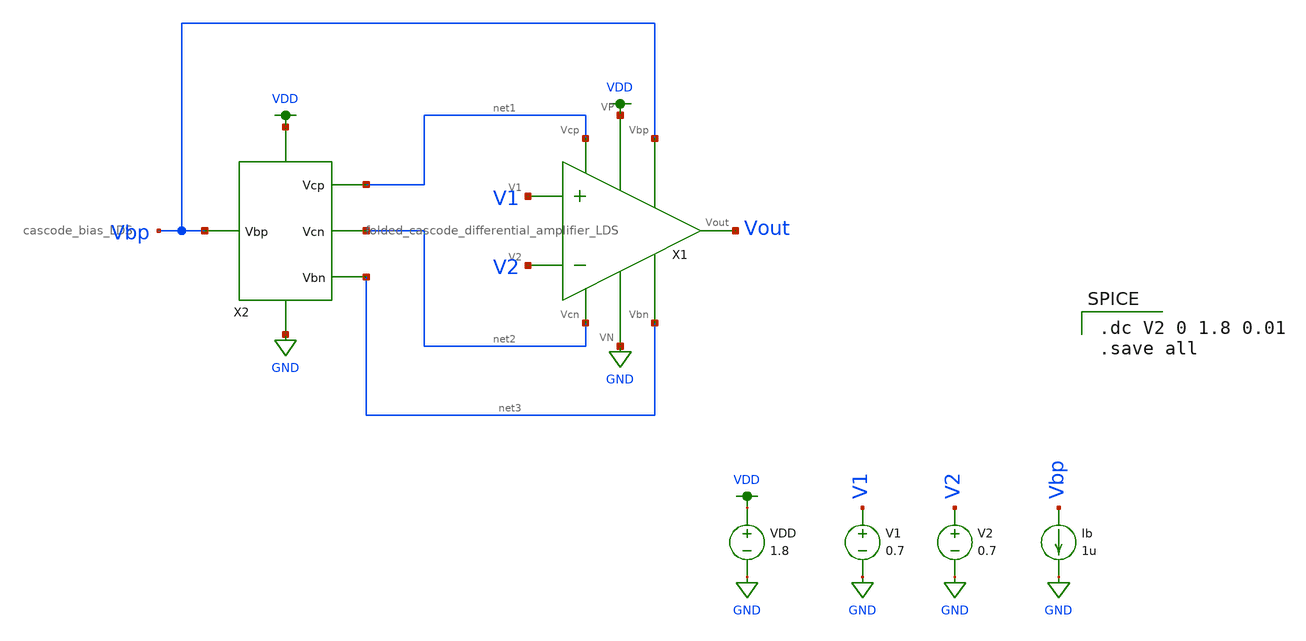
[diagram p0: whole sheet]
** sch_path: schematic/folded_cascode_simulation.sch
**.subckt folded_cascode_simulation
X1 VDD Vbp net1 Vout net3 net2 V1 V2 GND folded_cascode_differential_amplifier_LDS
X2 VDD net1 Vbp net2 net3 GND cascode_bias_LDS
VDD VDD GND 1.8
V1 V1 GND 0.7
V2 V2 GND 0.7
Ib Vbp GND 1u
**** begin user architecture code

.option wnflag=1
.lib ~/skywater/skywater-pdk/libraries/sky130_fd_pr_ngspice/latest/models/sky130.lib.spice tt


.dc V2 0 1.8 0.01
.save all

**** end user architecture code
**.ends

* expanding   symbol:
*+  /home/madvlsi/Documents/MADVLSI-MP3/schematic/folded_cascode_differential_amplifier_LDS.sym # of pins=9
** sym_path: schematic/folded_cascode_differential_amplifier_LDS.sym
** sch_path: schematic/folded_cascode_differential_amplifier_LDS.sch
.subckt folded_cascode_differential_amplifier_LDS VP Vbp Vcp Vout Vbn Vcn V1 V2 VN
*.ipin Vbn
*.ipin Vcn
*.ipin Vcp
*.ipin V2
*.ipin V1
*.ipin Vbp
*.iopin VP
*.iopin VN
*.opin Vout
XM5a net3 Vcn net6 GND sky130_fd_pr__nfet_01v8 L=0.5 W=6 nf=1 ad='int((nf+1)/2) * W/nf * 0.29' as='int((nf+2)/2) * W/nf * 0.29'
+ pd='2*int((nf+1)/2) * (W/nf + 0.29)' ps='2*int((nf+2)/2) * (W/nf + 0.29)' nrd='0.29 / W' nrs='0.29 / W'
+ sa=0 sb=0 sd=0 mult=1 m=1
XM1a net3 V1 net1 VDD sky130_fd_pr__pfet_01v8 L=0.5 W=3 nf=1 ad='int((nf+1)/2) * W/nf * 0.29' as='int((nf+2)/2) * W/nf * 0.29'
+ pd='2*int((nf+1)/2) * (W/nf + 0.29)' ps='2*int((nf+2)/2) * (W/nf + 0.29)' nrd='0.29 / W' nrs='0.29 / W'
+ sa=0 sb=0 sd=0 mult=1 m=1
XM2a net2 V2 net1 VDD sky130_fd_pr__pfet_01v8 L=0.5 W=3 nf=1 ad='int((nf+1)/2) * W/nf * 0.29' as='int((nf+2)/2) * W/nf * 0.29'
+ pd='2*int((nf+1)/2) * (W/nf + 0.29)' ps='2*int((nf+2)/2) * (W/nf + 0.29)' nrd='0.29 / W' nrs='0.29 / W'
+ sa=0 sb=0 sd=0 mult=1 m=1
XM2b net1 V2 net2 VDD sky130_fd_pr__pfet_01v8 L=0.5 W=3 nf=1 ad='int((nf+1)/2) * W/nf * 0.29' as='int((nf+2)/2) * W/nf * 0.29'
+ pd='2*int((nf+1)/2) * (W/nf + 0.29)' ps='2*int((nf+2)/2) * (W/nf + 0.29)' nrd='0.29 / W' nrs='0.29 / W'
+ sa=0 sb=0 sd=0 mult=1 m=1
XM1b net1 V1 net3 VDD sky130_fd_pr__pfet_01v8 L=0.5 W=3 nf=1 ad='int((nf+1)/2) * W/nf * 0.29' as='int((nf+2)/2) * W/nf * 0.29'
+ pd='2*int((nf+1)/2) * (W/nf + 0.29)' ps='2*int((nf+2)/2) * (W/nf + 0.29)' nrd='0.29 / W' nrs='0.29 / W'
+ sa=0 sb=0 sd=0 mult=1 m=1
XM1c net3 V1 net1 VDD sky130_fd_pr__pfet_01v8 L=0.5 W=3 nf=1 ad='int((nf+1)/2) * W/nf * 0.29' as='int((nf+2)/2) * W/nf * 0.29'
+ pd='2*int((nf+1)/2) * (W/nf + 0.29)' ps='2*int((nf+2)/2) * (W/nf + 0.29)' nrd='0.29 / W' nrs='0.29 / W'
+ sa=0 sb=0 sd=0 mult=1 m=1
XM2c net2 V2 net1 VDD sky130_fd_pr__pfet_01v8 L=0.5 W=3 nf=1 ad='int((nf+1)/2) * W/nf * 0.29' as='int((nf+2)/2) * W/nf * 0.29'
+ pd='2*int((nf+1)/2) * (W/nf + 0.29)' ps='2*int((nf+2)/2) * (W/nf + 0.29)' nrd='0.29 / W' nrs='0.29 / W'
+ sa=0 sb=0 sd=0 mult=1 m=1
XM2d net1 V2 net2 VDD sky130_fd_pr__pfet_01v8 L=0.5 W=3 nf=1 ad='int((nf+1)/2) * W/nf * 0.29' as='int((nf+2)/2) * W/nf * 0.29'
+ pd='2*int((nf+1)/2) * (W/nf + 0.29)' ps='2*int((nf+2)/2) * (W/nf + 0.29)' nrd='0.29 / W' nrs='0.29 / W'
+ sa=0 sb=0 sd=0 mult=1 m=1
XM1d net1 V1 net3 VDD sky130_fd_pr__pfet_01v8 L=0.5 W=3 nf=1 ad='int((nf+1)/2) * W/nf * 0.29' as='int((nf+2)/2) * W/nf * 0.29'
+ pd='2*int((nf+1)/2) * (W/nf + 0.29)' ps='2*int((nf+2)/2) * (W/nf + 0.29)' nrd='0.29 / W' nrs='0.29 / W'
+ sa=0 sb=0 sd=0 mult=1 m=1
XM11a VP Vbp net1 VDD sky130_fd_pr__pfet_01v8 L=0.5 W=1.5 nf=1 ad='int((nf+1)/2) * W/nf * 0.29' as='int((nf+2)/2) * W/nf * 0.29'
+ pd='2*int((nf+1)/2) * (W/nf + 0.29)' ps='2*int((nf+2)/2) * (W/nf + 0.29)' nrd='0.29 / W' nrs='0.29 / W'
+ sa=0 sb=0 sd=0 mult=1 m=1
XM11b net1 Vbp VP VDD sky130_fd_pr__pfet_01v8 L=0.5 W=1.5 nf=1 ad='int((nf+1)/2) * W/nf * 0.29' as='int((nf+2)/2) * W/nf * 0.29'
+ pd='2*int((nf+1)/2) * (W/nf + 0.29)' ps='2*int((nf+2)/2) * (W/nf + 0.29)' nrd='0.29 / W' nrs='0.29 / W'
+ sa=0 sb=0 sd=0 mult=1 m=1
XM11c VP Vbp net1 VDD sky130_fd_pr__pfet_01v8 L=0.5 W=1.5 nf=1 ad='int((nf+1)/2) * W/nf * 0.29' as='int((nf+2)/2) * W/nf * 0.29'
+ pd='2*int((nf+1)/2) * (W/nf + 0.29)' ps='2*int((nf+2)/2) * (W/nf + 0.29)' nrd='0.29 / W' nrs='0.29 / W'
+ sa=0 sb=0 sd=0 mult=1 m=1
XM11d net1 Vbp VP VDD sky130_fd_pr__pfet_01v8 L=0.5 W=1.5 nf=1 ad='int((nf+1)/2) * W/nf * 0.29' as='int((nf+2)/2) * W/nf * 0.29'
+ pd='2*int((nf+1)/2) * (W/nf + 0.29)' ps='2*int((nf+2)/2) * (W/nf + 0.29)' nrd='0.29 / W' nrs='0.29 / W'
+ sa=0 sb=0 sd=0 mult=1 m=1
XM11e VP Vbp net1 VDD sky130_fd_pr__pfet_01v8 L=0.5 W=1.5 nf=1 ad='int((nf+1)/2) * W/nf * 0.29' as='int((nf+2)/2) * W/nf * 0.29'
+ pd='2*int((nf+1)/2) * (W/nf + 0.29)' ps='2*int((nf+2)/2) * (W/nf + 0.29)' nrd='0.29 / W' nrs='0.29 / W'
+ sa=0 sb=0 sd=0 mult=1 m=1
XM11f net1 Vbp VP VDD sky130_fd_pr__pfet_01v8 L=0.5 W=1.5 nf=1 ad='int((nf+1)/2) * W/nf * 0.29' as='int((nf+2)/2) * W/nf * 0.29'
+ pd='2*int((nf+1)/2) * (W/nf + 0.29)' ps='2*int((nf+2)/2) * (W/nf + 0.29)' nrd='0.29 / W' nrs='0.29 / W'
+ sa=0 sb=0 sd=0 mult=1 m=1
XM11g VP Vbp net1 VDD sky130_fd_pr__pfet_01v8 L=0.5 W=1.5 nf=1 ad='int((nf+1)/2) * W/nf * 0.29' as='int((nf+2)/2) * W/nf * 0.29'
+ pd='2*int((nf+1)/2) * (W/nf + 0.29)' ps='2*int((nf+2)/2) * (W/nf + 0.29)' nrd='0.29 / W' nrs='0.29 / W'
+ sa=0 sb=0 sd=0 mult=1 m=1
XM11h net1 Vbp VP VDD sky130_fd_pr__pfet_01v8 L=0.5 W=1.5 nf=1 ad='int((nf+1)/2) * W/nf * 0.29' as='int((nf+2)/2) * W/nf * 0.29'
+ pd='2*int((nf+1)/2) * (W/nf + 0.29)' ps='2*int((nf+2)/2) * (W/nf + 0.29)' nrd='0.29 / W' nrs='0.29 / W'
+ sa=0 sb=0 sd=0 mult=1 m=1
XM3a VN Vbn net3 GND sky130_fd_pr__nfet_01v8 L=0.5 W=6 nf=1 ad='int((nf+1)/2) * W/nf * 0.29' as='int((nf+2)/2) * W/nf * 0.29'
+ pd='2*int((nf+1)/2) * (W/nf + 0.29)' ps='2*int((nf+2)/2) * (W/nf + 0.29)' nrd='0.29 / W' nrs='0.29 / W'
+ sa=0 sb=0 sd=0 mult=1 m=1
XM4a net2 Vbn VN GND sky130_fd_pr__nfet_01v8 L=0.5 W=6 nf=1 ad='int((nf+1)/2) * W/nf * 0.29' as='int((nf+2)/2) * W/nf * 0.29'
+ pd='2*int((nf+1)/2) * (W/nf + 0.29)' ps='2*int((nf+2)/2) * (W/nf + 0.29)' nrd='0.29 / W' nrs='0.29 / W'
+ sa=0 sb=0 sd=0 mult=1 m=1
XM6a Vout Vcn net2 GND sky130_fd_pr__nfet_01v8 L=0.5 W=6 nf=1 ad='int((nf+1)/2) * W/nf * 0.29' as='int((nf+2)/2) * W/nf * 0.29'
+ pd='2*int((nf+1)/2) * (W/nf + 0.29)' ps='2*int((nf+2)/2) * (W/nf + 0.29)' nrd='0.29 / W' nrs='0.29 / W'
+ sa=0 sb=0 sd=0 mult=1 m=1
XM6b net2 Vcn Vout GND sky130_fd_pr__nfet_01v8 L=0.5 W=6 nf=1 ad='int((nf+1)/2) * W/nf * 0.29' as='int((nf+2)/2) * W/nf * 0.29'
+ pd='2*int((nf+1)/2) * (W/nf + 0.29)' ps='2*int((nf+2)/2) * (W/nf + 0.29)' nrd='0.29 / W' nrs='0.29 / W'
+ sa=0 sb=0 sd=0 mult=1 m=1
XM4b VN Vbn net2 GND sky130_fd_pr__nfet_01v8 L=0.5 W=6 nf=1 ad='int((nf+1)/2) * W/nf * 0.29' as='int((nf+2)/2) * W/nf * 0.29'
+ pd='2*int((nf+1)/2) * (W/nf + 0.29)' ps='2*int((nf+2)/2) * (W/nf + 0.29)' nrd='0.29 / W' nrs='0.29 / W'
+ sa=0 sb=0 sd=0 mult=1 m=1
XM3b net3 Vbn VN GND sky130_fd_pr__nfet_01v8 L=0.5 W=6 nf=1 ad='int((nf+1)/2) * W/nf * 0.29' as='int((nf+2)/2) * W/nf * 0.29'
+ pd='2*int((nf+1)/2) * (W/nf + 0.29)' ps='2*int((nf+2)/2) * (W/nf + 0.29)' nrd='0.29 / W' nrs='0.29 / W'
+ sa=0 sb=0 sd=0 mult=1 m=1
XM5b net6 Vcn net3 GND sky130_fd_pr__nfet_01v8 L=0.5 W=6 nf=1 ad='int((nf+1)/2) * W/nf * 0.29' as='int((nf+2)/2) * W/nf * 0.29'
+ pd='2*int((nf+1)/2) * (W/nf + 0.29)' ps='2*int((nf+2)/2) * (W/nf + 0.29)' nrd='0.29 / W' nrs='0.29 / W'
+ sa=0 sb=0 sd=0 mult=1 m=1
XM10a Vout Vcp net4 VDD sky130_fd_pr__pfet_01v8 L=0.5 W=6 nf=1 ad='int((nf+1)/2) * W/nf * 0.29' as='int((nf+2)/2) * W/nf * 0.29'
+ pd='2*int((nf+1)/2) * (W/nf + 0.29)' ps='2*int((nf+2)/2) * (W/nf + 0.29)' nrd='0.29 / W' nrs='0.29 / W'
+ sa=0 sb=0 sd=0 mult=1 m=1
XM8a net4 net6 VP VDD sky130_fd_pr__pfet_01v8 L=0.5 W=6 nf=1 ad='int((nf+1)/2) * W/nf * 0.29' as='int((nf+2)/2) * W/nf * 0.29'
+ pd='2*int((nf+1)/2) * (W/nf + 0.29)' ps='2*int((nf+2)/2) * (W/nf + 0.29)' nrd='0.29 / W' nrs='0.29 / W'
+ sa=0 sb=0 sd=0 mult=1 m=1
XM7a VP net6 net5 VDD sky130_fd_pr__pfet_01v8 L=0.5 W=6 nf=1 ad='int((nf+1)/2) * W/nf * 0.29' as='int((nf+2)/2) * W/nf * 0.29'
+ pd='2*int((nf+1)/2) * (W/nf + 0.29)' ps='2*int((nf+2)/2) * (W/nf + 0.29)' nrd='0.29 / W' nrs='0.29 / W'
+ sa=0 sb=0 sd=0 mult=1 m=1
XM9a net5 Vcp net6 VDD sky130_fd_pr__pfet_01v8 L=0.5 W=6 nf=1 ad='int((nf+1)/2) * W/nf * 0.29' as='int((nf+2)/2) * W/nf * 0.29'
+ pd='2*int((nf+1)/2) * (W/nf + 0.29)' ps='2*int((nf+2)/2) * (W/nf + 0.29)' nrd='0.29 / W' nrs='0.29 / W'
+ sa=0 sb=0 sd=0 mult=1 m=1
XM9b net6 Vcp net5 VDD sky130_fd_pr__pfet_01v8 L=0.5 W=6 nf=1 ad='int((nf+1)/2) * W/nf * 0.29' as='int((nf+2)/2) * W/nf * 0.29'
+ pd='2*int((nf+1)/2) * (W/nf + 0.29)' ps='2*int((nf+2)/2) * (W/nf + 0.29)' nrd='0.29 / W' nrs='0.29 / W'
+ sa=0 sb=0 sd=0 mult=1 m=1
XM7b net5 net6 VP VDD sky130_fd_pr__pfet_01v8 L=0.5 W=6 nf=1 ad='int((nf+1)/2) * W/nf * 0.29' as='int((nf+2)/2) * W/nf * 0.29'
+ pd='2*int((nf+1)/2) * (W/nf + 0.29)' ps='2*int((nf+2)/2) * (W/nf + 0.29)' nrd='0.29 / W' nrs='0.29 / W'
+ sa=0 sb=0 sd=0 mult=1 m=1
XM8b VP net6 net4 VDD sky130_fd_pr__pfet_01v8 L=0.5 W=6 nf=1 ad='int((nf+1)/2) * W/nf * 0.29' as='int((nf+2)/2) * W/nf * 0.29'
+ pd='2*int((nf+1)/2) * (W/nf + 0.29)' ps='2*int((nf+2)/2) * (W/nf + 0.29)' nrd='0.29 / W' nrs='0.29 / W'
+ sa=0 sb=0 sd=0 mult=1 m=1
XM10b net4 Vcp Vout VDD sky130_fd_pr__pfet_01v8 L=0.5 W=6 nf=1 ad='int((nf+1)/2) * W/nf * 0.29' as='int((nf+2)/2) * W/nf * 0.29'
+ pd='2*int((nf+1)/2) * (W/nf + 0.29)' ps='2*int((nf+2)/2) * (W/nf + 0.29)' nrd='0.29 / W' nrs='0.29 / W'
+ sa=0 sb=0 sd=0 mult=1 m=1
XM15 net3 VP VP VDD sky130_fd_pr__pfet_01v8 L=0.5 W=3 nf=1 ad='int((nf+1)/2) * W/nf * 0.29' as='int((nf+2)/2) * W/nf * 0.29'
+ pd='2*int((nf+1)/2) * (W/nf + 0.29)' ps='2*int((nf+2)/2) * (W/nf + 0.29)' nrd='0.29 / W' nrs='0.29 / W'
+ sa=0 sb=0 sd=0 mult=1 m=1
XM14 VP VP net3 VDD sky130_fd_pr__pfet_01v8 L=0.5 W=3 nf=1 ad='int((nf+1)/2) * W/nf * 0.29' as='int((nf+2)/2) * W/nf * 0.29'
+ pd='2*int((nf+1)/2) * (W/nf + 0.29)' ps='2*int((nf+2)/2) * (W/nf + 0.29)' nrd='0.29 / W' nrs='0.29 / W'
+ sa=0 sb=0 sd=0 mult=1 m=1
XM13 VP VP VP VDD sky130_fd_pr__pfet_01v8 L=0.5 W=1.5 nf=1 ad='int((nf+1)/2) * W/nf * 0.29' as='int((nf+2)/2) * W/nf * 0.29'
+ pd='2*int((nf+1)/2) * (W/nf + 0.29)' ps='2*int((nf+2)/2) * (W/nf + 0.29)' nrd='0.29 / W' nrs='0.29 / W'
+ sa=0 sb=0 sd=0 mult=1 m=1
XM12 VP VP VP VDD sky130_fd_pr__pfet_01v8 L=0.5 W=1.5 nf=1 ad='int((nf+1)/2) * W/nf * 0.29' as='int((nf+2)/2) * W/nf * 0.29'
+ pd='2*int((nf+1)/2) * (W/nf + 0.29)' ps='2*int((nf+2)/2) * (W/nf + 0.29)' nrd='0.29 / W' nrs='0.29 / W'
+ sa=0 sb=0 sd=0 mult=1 m=1
XM16 VP VP Vout VDD sky130_fd_pr__pfet_01v8 L=0.5 W=6 nf=1 ad='int((nf+1)/2) * W/nf * 0.29' as='int((nf+2)/2) * W/nf * 0.29'
+ pd='2*int((nf+1)/2) * (W/nf + 0.29)' ps='2*int((nf+2)/2) * (W/nf + 0.29)' nrd='0.29 / W' nrs='0.29 / W'
+ sa=0 sb=0 sd=0 mult=1 m=1
XM17 Vout VP VP VDD sky130_fd_pr__pfet_01v8 L=0.5 W=6 nf=1 ad='int((nf+1)/2) * W/nf * 0.29' as='int((nf+2)/2) * W/nf * 0.29'
+ pd='2*int((nf+1)/2) * (W/nf + 0.29)' ps='2*int((nf+2)/2) * (W/nf + 0.29)' nrd='0.29 / W' nrs='0.29 / W'
+ sa=0 sb=0 sd=0 mult=1 m=1
XM19 VN VN net6 GND sky130_fd_pr__nfet_01v8 L=0.5 W=6 nf=1 ad='int((nf+1)/2) * W/nf * 0.29' as='int((nf+2)/2) * W/nf * 0.29'
+ pd='2*int((nf+1)/2) * (W/nf + 0.29)' ps='2*int((nf+2)/2) * (W/nf + 0.29)' nrd='0.29 / W' nrs='0.29 / W'
+ sa=0 sb=0 sd=0 mult=1 m=1
XM18 net6 VN VN GND sky130_fd_pr__nfet_01v8 L=0.5 W=6 nf=1 ad='int((nf+1)/2) * W/nf * 0.29' as='int((nf+2)/2) * W/nf * 0.29'
+ pd='2*int((nf+1)/2) * (W/nf + 0.29)' ps='2*int((nf+2)/2) * (W/nf + 0.29)' nrd='0.29 / W' nrs='0.29 / W'
+ sa=0 sb=0 sd=0 mult=1 m=1
.ends


* expanding   symbol:  /home/madvlsi/Documents/MADVLSI-MP3/schematic/cascode_bias_LDS.sym # of
*+ pins=6
** sym_path: schematic/cascode_bias_LDS.sym
** sch_path: schematic/cascode_bias_LDS.sch
.subckt cascode_bias_LDS VP Vcp Vbp Vcn Vbn VN
*.iopin VP
*.iopin VN
*.opin Vcp
*.opin Vbn
*.opin Vcn
*.iopin Vbp
XM1a VP Vbp Vbp VDD sky130_fd_pr__pfet_01v8 L=0.5 W=6 nf=1 ad='int((nf+1)/2) * W/nf * 0.29' as='int((nf+2)/2) * W/nf * 0.29'
+ pd='2*int((nf+1)/2) * (W/nf + 0.29)' ps='2*int((nf+2)/2) * (W/nf + 0.29)' nrd='0.29 / W' nrs='0.29 / W'
+ sa=0 sb=0 sd=0 mult=1 m=1
XM2a Vbn Vbp VP VDD sky130_fd_pr__pfet_01v8 L=0.5 W=6 nf=1 ad='int((nf+1)/2) * W/nf * 0.29' as='int((nf+2)/2) * W/nf * 0.29'
+ pd='2*int((nf+1)/2) * (W/nf + 0.29)' ps='2*int((nf+2)/2) * (W/nf + 0.29)' nrd='0.29 / W' nrs='0.29 / W'
+ sa=0 sb=0 sd=0 mult=1 m=1
XM3a VP Vbp Vcn VDD sky130_fd_pr__pfet_01v8 L=0.5 W=6 nf=1 ad='int((nf+1)/2) * W/nf * 0.29' as='int((nf+2)/2) * W/nf * 0.29'
+ pd='2*int((nf+1)/2) * (W/nf + 0.29)' ps='2*int((nf+2)/2) * (W/nf + 0.29)' nrd='0.29 / W' nrs='0.29 / W'
+ sa=0 sb=0 sd=0 mult=1 m=1
XM4a net1 Vbp VP VDD sky130_fd_pr__pfet_01v8 L=0.5 W=6 nf=1 ad='int((nf+1)/2) * W/nf * 0.29' as='int((nf+2)/2) * W/nf * 0.29'
+ pd='2*int((nf+1)/2) * (W/nf + 0.29)' ps='2*int((nf+2)/2) * (W/nf + 0.29)' nrd='0.29 / W' nrs='0.29 / W'
+ sa=0 sb=0 sd=0 mult=1 m=1
XM4b VP Vbp net1 VDD sky130_fd_pr__pfet_01v8 L=0.5 W=6 nf=1 ad='int((nf+1)/2) * W/nf * 0.29' as='int((nf+2)/2) * W/nf * 0.29'
+ pd='2*int((nf+1)/2) * (W/nf + 0.29)' ps='2*int((nf+2)/2) * (W/nf + 0.29)' nrd='0.29 / W' nrs='0.29 / W'
+ sa=0 sb=0 sd=0 mult=1 m=1
XM3b Vcn Vbp VP VDD sky130_fd_pr__pfet_01v8 L=0.5 W=6 nf=1 ad='int((nf+1)/2) * W/nf * 0.29' as='int((nf+2)/2) * W/nf * 0.29'
+ pd='2*int((nf+1)/2) * (W/nf + 0.29)' ps='2*int((nf+2)/2) * (W/nf + 0.29)' nrd='0.29 / W' nrs='0.29 / W'
+ sa=0 sb=0 sd=0 mult=1 m=1
XM2b VP Vbp Vbn VDD sky130_fd_pr__pfet_01v8 L=0.5 W=6 nf=1 ad='int((nf+1)/2) * W/nf * 0.29' as='int((nf+2)/2) * W/nf * 0.29'
+ pd='2*int((nf+1)/2) * (W/nf + 0.29)' ps='2*int((nf+2)/2) * (W/nf + 0.29)' nrd='0.29 / W' nrs='0.29 / W'
+ sa=0 sb=0 sd=0 mult=1 m=1
XM1b Vbp Vbp VP VDD sky130_fd_pr__pfet_01v8 L=0.5 W=6 nf=1 ad='int((nf+1)/2) * W/nf * 0.29' as='int((nf+2)/2) * W/nf * 0.29'
+ pd='2*int((nf+1)/2) * (W/nf + 0.29)' ps='2*int((nf+2)/2) * (W/nf + 0.29)' nrd='0.29 / W' nrs='0.29 / W'
+ sa=0 sb=0 sd=0 mult=1 m=1
XM7a net3 net3 net2 VDD sky130_fd_pr__pfet_01v8 L=0.5 W=6 nf=1 ad='int((nf+1)/2) * W/nf * 0.29' as='int((nf+2)/2) * W/nf * 0.29'
+ pd='2*int((nf+1)/2) * (W/nf + 0.29)' ps='2*int((nf+2)/2) * (W/nf + 0.29)' nrd='0.29 / W' nrs='0.29 / W'
+ sa=0 sb=0 sd=0 mult=1 m=1
XM6a net2 net3 VP VDD sky130_fd_pr__pfet_01v8 L=0.5 W=6 nf=1 ad='int((nf+1)/2) * W/nf * 0.29' as='int((nf+2)/2) * W/nf * 0.29'
+ pd='2*int((nf+1)/2) * (W/nf + 0.29)' ps='2*int((nf+2)/2) * (W/nf + 0.29)' nrd='0.29 / W' nrs='0.29 / W'
+ sa=0 sb=0 sd=0 mult=1 m=1
XM5a Vcp Vcp net2 VDD sky130_fd_pr__pfet_01v8 L=0.5 W=6 nf=1 ad='int((nf+1)/2) * W/nf * 0.29' as='int((nf+2)/2) * W/nf * 0.29'
+ pd='2*int((nf+1)/2) * (W/nf + 0.29)' ps='2*int((nf+2)/2) * (W/nf + 0.29)' nrd='0.29 / W' nrs='0.29 / W'
+ sa=0 sb=0 sd=0 mult=1 m=1
XM5b net2 Vcp Vcp VDD sky130_fd_pr__pfet_01v8 L=0.5 W=6 nf=1 ad='int((nf+1)/2) * W/nf * 0.29' as='int((nf+2)/2) * W/nf * 0.29'
+ pd='2*int((nf+1)/2) * (W/nf + 0.29)' ps='2*int((nf+2)/2) * (W/nf + 0.29)' nrd='0.29 / W' nrs='0.29 / W'
+ sa=0 sb=0 sd=0 mult=1 m=1
XM6b VP net3 net2 VDD sky130_fd_pr__pfet_01v8 L=0.5 W=6 nf=1 ad='int((nf+1)/2) * W/nf * 0.29' as='int((nf+2)/2) * W/nf * 0.29'
+ pd='2*int((nf+1)/2) * (W/nf + 0.29)' ps='2*int((nf+2)/2) * (W/nf + 0.29)' nrd='0.29 / W' nrs='0.29 / W'
+ sa=0 sb=0 sd=0 mult=1 m=1
XM7b net2 net3 net3 VDD sky130_fd_pr__pfet_01v8 L=0.5 W=6 nf=1 ad='int((nf+1)/2) * W/nf * 0.29' as='int((nf+2)/2) * W/nf * 0.29'
+ pd='2*int((nf+1)/2) * (W/nf + 0.29)' ps='2*int((nf+2)/2) * (W/nf + 0.29)' nrd='0.29 / W' nrs='0.29 / W'
+ sa=0 sb=0 sd=0 mult=1 m=1
XM8a Vbn Vbn VN GND sky130_fd_pr__nfet_01v8 L=0.5 W=6 nf=1 ad='int((nf+1)/2) * W/nf * 0.29' as='int((nf+2)/2) * W/nf * 0.29'
+ pd='2*int((nf+1)/2) * (W/nf + 0.29)' ps='2*int((nf+2)/2) * (W/nf + 0.29)' nrd='0.29 / W' nrs='0.29 / W'
+ sa=0 sb=0 sd=0 mult=1 m=1
XM8b VN Vbn Vbn GND sky130_fd_pr__nfet_01v8 L=0.5 W=6 nf=1 ad='int((nf+1)/2) * W/nf * 0.29' as='int((nf+2)/2) * W/nf * 0.29'
+ pd='2*int((nf+1)/2) * (W/nf + 0.29)' ps='2*int((nf+2)/2) * (W/nf + 0.29)' nrd='0.29 / W' nrs='0.29 / W'
+ sa=0 sb=0 sd=0 mult=1 m=1
XM10a VN Vbn net3 GND sky130_fd_pr__nfet_01v8 L=0.5 W=6 nf=1 ad='int((nf+1)/2) * W/nf * 0.29' as='int((nf+2)/2) * W/nf * 0.29'
+ pd='2*int((nf+1)/2) * (W/nf + 0.29)' ps='2*int((nf+2)/2) * (W/nf + 0.29)' nrd='0.29 / W' nrs='0.29 / W'
+ sa=0 sb=0 sd=0 mult=1 m=1
XM9a Vcp Vbn VN GND sky130_fd_pr__nfet_01v8 L=0.5 W=6 nf=1 ad='int((nf+1)/2) * W/nf * 0.29' as='int((nf+2)/2) * W/nf * 0.29'
+ pd='2*int((nf+1)/2) * (W/nf + 0.29)' ps='2*int((nf+2)/2) * (W/nf + 0.29)' nrd='0.29 / W' nrs='0.29 / W'
+ sa=0 sb=0 sd=0 mult=1 m=1
XM9b VN Vbn Vcp GND sky130_fd_pr__nfet_01v8 L=0.5 W=6 nf=1 ad='int((nf+1)/2) * W/nf * 0.29' as='int((nf+2)/2) * W/nf * 0.29'
+ pd='2*int((nf+1)/2) * (W/nf + 0.29)' ps='2*int((nf+2)/2) * (W/nf + 0.29)' nrd='0.29 / W' nrs='0.29 / W'
+ sa=0 sb=0 sd=0 mult=1 m=1
XM10b net3 Vbn VN GND sky130_fd_pr__nfet_01v8 L=0.5 W=6 nf=1 ad='int((nf+1)/2) * W/nf * 0.29' as='int((nf+2)/2) * W/nf * 0.29'
+ pd='2*int((nf+1)/2) * (W/nf + 0.29)' ps='2*int((nf+2)/2) * (W/nf + 0.29)' nrd='0.29 / W' nrs='0.29 / W'
+ sa=0 sb=0 sd=0 mult=1 m=1
XM11a Vcn Vcn net4 GND sky130_fd_pr__nfet_01v8 L=0.5 W=6 nf=1 ad='int((nf+1)/2) * W/nf * 0.29' as='int((nf+2)/2) * W/nf * 0.29'
+ pd='2*int((nf+1)/2) * (W/nf + 0.29)' ps='2*int((nf+2)/2) * (W/nf + 0.29)' nrd='0.29 / W' nrs='0.29 / W'
+ sa=0 sb=0 sd=0 mult=1 m=1
XM11b net4 Vcn Vcn GND sky130_fd_pr__nfet_01v8 L=0.5 W=6 nf=1 ad='int((nf+1)/2) * W/nf * 0.29' as='int((nf+2)/2) * W/nf * 0.29'
+ pd='2*int((nf+1)/2) * (W/nf + 0.29)' ps='2*int((nf+2)/2) * (W/nf + 0.29)' nrd='0.29 / W' nrs='0.29 / W'
+ sa=0 sb=0 sd=0 mult=1 m=1
XM13a net1 net1 net4 GND sky130_fd_pr__nfet_01v8 L=0.5 W=6 nf=1 ad='int((nf+1)/2) * W/nf * 0.29' as='int((nf+2)/2) * W/nf * 0.29'
+ pd='2*int((nf+1)/2) * (W/nf + 0.29)' ps='2*int((nf+2)/2) * (W/nf + 0.29)' nrd='0.29 / W' nrs='0.29 / W'
+ sa=0 sb=0 sd=0 mult=1 m=1
XM12a net4 net1 VN GND sky130_fd_pr__nfet_01v8 L=0.5 W=6 nf=1 ad='int((nf+1)/2) * W/nf * 0.29' as='int((nf+2)/2) * W/nf * 0.29'
+ pd='2*int((nf+1)/2) * (W/nf + 0.29)' ps='2*int((nf+2)/2) * (W/nf + 0.29)' nrd='0.29 / W' nrs='0.29 / W'
+ sa=0 sb=0 sd=0 mult=1 m=1
XM12b VN net1 net4 GND sky130_fd_pr__nfet_01v8 L=0.5 W=6 nf=1 ad='int((nf+1)/2) * W/nf * 0.29' as='int((nf+2)/2) * W/nf * 0.29'
+ pd='2*int((nf+1)/2) * (W/nf + 0.29)' ps='2*int((nf+2)/2) * (W/nf + 0.29)' nrd='0.29 / W' nrs='0.29 / W'
+ sa=0 sb=0 sd=0 mult=1 m=1
XM13b net4 net1 net1 GND sky130_fd_pr__nfet_01v8 L=0.5 W=6 nf=1 ad='int((nf+1)/2) * W/nf * 0.29' as='int((nf+2)/2) * W/nf * 0.29'
+ pd='2*int((nf+1)/2) * (W/nf + 0.29)' ps='2*int((nf+2)/2) * (W/nf + 0.29)' nrd='0.29 / W' nrs='0.29 / W'
+ sa=0 sb=0 sd=0 mult=1 m=1
XM15 Vbp VP VP VDD sky130_fd_pr__pfet_01v8 L=0.5 W=6 nf=1 ad='int((nf+1)/2) * W/nf * 0.29' as='int((nf+2)/2) * W/nf * 0.29'
+ pd='2*int((nf+1)/2) * (W/nf + 0.29)' ps='2*int((nf+2)/2) * (W/nf + 0.29)' nrd='0.29 / W' nrs='0.29 / W'
+ sa=0 sb=0 sd=0 mult=1 m=1
XM25 net4 VN VN GND sky130_fd_pr__nfet_01v8 L=0.5 W=6 nf=1 ad='int((nf+1)/2) * W/nf * 0.29' as='int((nf+2)/2) * W/nf * 0.29'
+ pd='2*int((nf+1)/2) * (W/nf + 0.29)' ps='2*int((nf+2)/2) * (W/nf + 0.29)' nrd='0.29 / W' nrs='0.29 / W'
+ sa=0 sb=0 sd=0 mult=1 m=1
XM24 VN VN VN GND sky130_fd_pr__nfet_01v8 L=0.5 W=6 nf=1 ad='int((nf+1)/2) * W/nf * 0.29' as='int((nf+2)/2) * W/nf * 0.29'
+ pd='2*int((nf+1)/2) * (W/nf + 0.29)' ps='2*int((nf+2)/2) * (W/nf + 0.29)' nrd='0.29 / W' nrs='0.29 / W'
+ sa=0 sb=0 sd=0 mult=1 m=1
XM26 VN VN net4 GND sky130_fd_pr__nfet_01v8 L=0.5 W=6 nf=1 ad='int((nf+1)/2) * W/nf * 0.29' as='int((nf+2)/2) * W/nf * 0.29'
+ pd='2*int((nf+1)/2) * (W/nf + 0.29)' ps='2*int((nf+2)/2) * (W/nf + 0.29)' nrd='0.29 / W' nrs='0.29 / W'
+ sa=0 sb=0 sd=0 mult=1 m=1
XM27 VN VN VN GND sky130_fd_pr__nfet_01v8 L=0.5 W=6 nf=1 ad='int((nf+1)/2) * W/nf * 0.29' as='int((nf+2)/2) * W/nf * 0.29'
+ pd='2*int((nf+1)/2) * (W/nf + 0.29)' ps='2*int((nf+2)/2) * (W/nf + 0.29)' nrd='0.29 / W' nrs='0.29 / W'
+ sa=0 sb=0 sd=0 mult=1 m=1
XM21 net3 VN VN GND sky130_fd_pr__nfet_01v8 L=0.5 W=6 nf=1 ad='int((nf+1)/2) * W/nf * 0.29' as='int((nf+2)/2) * W/nf * 0.29'
+ pd='2*int((nf+1)/2) * (W/nf + 0.29)' ps='2*int((nf+2)/2) * (W/nf + 0.29)' nrd='0.29 / W' nrs='0.29 / W'
+ sa=0 sb=0 sd=0 mult=1 m=1
XM20 VN VN VN GND sky130_fd_pr__nfet_01v8 L=0.5 W=6 nf=1 ad='int((nf+1)/2) * W/nf * 0.29' as='int((nf+2)/2) * W/nf * 0.29'
+ pd='2*int((nf+1)/2) * (W/nf + 0.29)' ps='2*int((nf+2)/2) * (W/nf + 0.29)' nrd='0.29 / W' nrs='0.29 / W'
+ sa=0 sb=0 sd=0 mult=1 m=1
XM23 VN VN VN GND sky130_fd_pr__nfet_01v8 L=0.5 W=6 nf=1 ad='int((nf+1)/2) * W/nf * 0.29' as='int((nf+2)/2) * W/nf * 0.29'
+ pd='2*int((nf+1)/2) * (W/nf + 0.29)' ps='2*int((nf+2)/2) * (W/nf + 0.29)' nrd='0.29 / W' nrs='0.29 / W'
+ sa=0 sb=0 sd=0 mult=1 m=1
XM22 VN VN net3 GND sky130_fd_pr__nfet_01v8 L=0.5 W=6 nf=1 ad='int((nf+1)/2) * W/nf * 0.29' as='int((nf+2)/2) * W/nf * 0.29'
+ pd='2*int((nf+1)/2) * (W/nf + 0.29)' ps='2*int((nf+2)/2) * (W/nf + 0.29)' nrd='0.29 / W' nrs='0.29 / W'
+ sa=0 sb=0 sd=0 mult=1 m=1
XM14 VP VP Vbp VDD sky130_fd_pr__pfet_01v8 L=0.5 W=6 nf=1 ad='int((nf+1)/2) * W/nf * 0.29' as='int((nf+2)/2) * W/nf * 0.29'
+ pd='2*int((nf+1)/2) * (W/nf + 0.29)' ps='2*int((nf+2)/2) * (W/nf + 0.29)' nrd='0.29 / W' nrs='0.29 / W'
+ sa=0 sb=0 sd=0 mult=1 m=1
XM17 net2 VP VP VDD sky130_fd_pr__pfet_01v8 L=0.5 W=6 nf=1 ad='int((nf+1)/2) * W/nf * 0.29' as='int((nf+2)/2) * W/nf * 0.29'
+ pd='2*int((nf+1)/2) * (W/nf + 0.29)' ps='2*int((nf+2)/2) * (W/nf + 0.29)' nrd='0.29 / W' nrs='0.29 / W'
+ sa=0 sb=0 sd=0 mult=1 m=1
XM16 VP VP VP VDD sky130_fd_pr__pfet_01v8 L=0.5 W=6 nf=1 ad='int((nf+1)/2) * W/nf * 0.29' as='int((nf+2)/2) * W/nf * 0.29'
+ pd='2*int((nf+1)/2) * (W/nf + 0.29)' ps='2*int((nf+2)/2) * (W/nf + 0.29)' nrd='0.29 / W' nrs='0.29 / W'
+ sa=0 sb=0 sd=0 mult=1 m=1
XM18 VP VP net2 VDD sky130_fd_pr__pfet_01v8 L=0.5 W=6 nf=1 ad='int((nf+1)/2) * W/nf * 0.29' as='int((nf+2)/2) * W/nf * 0.29'
+ pd='2*int((nf+1)/2) * (W/nf + 0.29)' ps='2*int((nf+2)/2) * (W/nf + 0.29)' nrd='0.29 / W' nrs='0.29 / W'
+ sa=0 sb=0 sd=0 mult=1 m=1
XM1 VP VP VP VDD sky130_fd_pr__pfet_01v8 L=0.5 W=6 nf=1 ad='int((nf+1)/2) * W/nf * 0.29' as='int((nf+2)/2) * W/nf * 0.29'
+ pd='2*int((nf+1)/2) * (W/nf + 0.29)' ps='2*int((nf+2)/2) * (W/nf + 0.29)' nrd='0.29 / W' nrs='0.29 / W'
+ sa=0 sb=0 sd=0 mult=1 m=1
.ends

.GLOBAL GND
.GLOBAL VDD
.end
